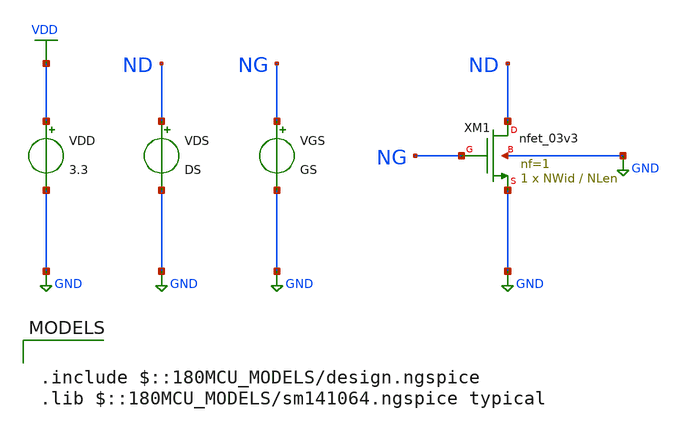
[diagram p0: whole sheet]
** sch_path: Design_Files/IC Design/Schematic/Gm_Id/NMOS_Gm_Id.sch
**.subckt NMOS_Gm_Id
XM1 ND NG GND GND nfet_03v3 L=NLen W=NWid nf=1 ad='int((nf+1)/2) * W/nf * 0.18u' as='int((nf+2)/2) * W/nf * 0.18u'
+ pd='2*int((nf+1)/2) * (W/nf + 0.18u)' ps='2*int((nf+2)/2) * (W/nf + 0.18u)' nrd='0.18u / W' nrs='0.18u / W'
+ sa=0 sb=0 sd=0 m=1
VGS NG GND GS
.save i(vgs)
VDS ND GND DS
.save i(vds)
VDD VDD GND 3.3
**** begin user architecture code



.param NWid=10u
.param NLen=1u
.param GS=0
.param DS=1.65

.control

shell mkdir -p /foss/designs/ecg_acquisition_ic/Measurement_Results/IC_Simulation/Gm_Id/NMOS_Gm_Id/

set wr_vecnames
set wr_singlescale

* =========================================================
* NMOS gm/Id 2D DC sweep
* W fixed at 10u
* Sweep VGS and VDS
* Export VGS, VDS, ID, ID/W for MATLAB
* =========================================================

alterparam NLen = 0.28u
reset
save all
dc VGS 0 3.3 0.01 VDS 0 3.3 0.01
let vgs_out = v(ng)
let vds_out = v(nd)
let id = abs(vds#branch)
let id_w = id/10e-6
wrdata
+ /foss/designs/ecg_acquisition_ic/Measurement_Results/IC_Simulation/Gm_Id/NMOS_Gm_Id/nmos_L0p28u_W10u.txt vgs_out vds_out id id_w

alterparam NLen = 0.5u
reset
save all
dc VGS 0 3.3 0.01 VDS 0 3.3 0.01
let vgs_out = v(ng)
let vds_out = v(nd)
let id = abs(vds#branch)
let id_w = id/10e-6
wrdata
+ /foss/designs/ecg_acquisition_ic/Measurement_Results/IC_Simulation/Gm_Id/NMOS_Gm_Id/nmos_L0p5u_W10u.txt vgs_out vds_out id id_w

alterparam NLen = 1u
reset
save all
dc VGS 0 3.3 0.01 VDS 0 3.3 0.01
let vgs_out = v(ng)
let vds_out = v(nd)
let id = abs(vds#branch)
let id_w = id/10e-6
wrdata
+ /foss/designs/ecg_acquisition_ic/Measurement_Results/IC_Simulation/Gm_Id/NMOS_Gm_Id/nmos_L1u_W10u.txt vgs_out vds_out id id_w

alterparam NLen = 1.5u
reset
save all
dc VGS 0 3.3 0.01 VDS 0 3.3 0.01
let vgs_out = v(ng)
let vds_out = v(nd)
let id = abs(vds#branch)
let id_w = id/10e-6
wrdata
+ /foss/designs/ecg_acquisition_ic/Measurement_Results/IC_Simulation/Gm_Id/NMOS_Gm_Id/nmos_L1p5u_W10u.txt vgs_out vds_out id id_w

alterparam NLen = 2u
reset
save all
dc VGS 0 3.3 0.01 VDS 0 3.3 0.01
let vgs_out = v(ng)
let vds_out = v(nd)
let id = abs(vds#branch)
let id_w = id/10e-6
wrdata
+ /foss/designs/ecg_acquisition_ic/Measurement_Results/IC_Simulation/Gm_Id/NMOS_Gm_Id/nmos_L2u_W10u.txt vgs_out vds_out id id_w

alterparam NLen = 3u
reset
save all
dc VGS 0 3.3 0.01 VDS 0 3.3 0.01
let vgs_out = v(ng)
let vds_out = v(nd)
let id = abs(vds#branch)
let id_w = id/10e-6
wrdata
+ /foss/designs/ecg_acquisition_ic/Measurement_Results/IC_Simulation/Gm_Id/NMOS_Gm_Id/nmos_L3u_W10u.txt vgs_out vds_out id id_w

.endc



.include $::180MCU_MODELS/design.ngspice
.lib $::180MCU_MODELS/sm141064.ngspice typical

**** end user architecture code
**.ends
.GLOBAL GND
.GLOBAL VDD
.end
